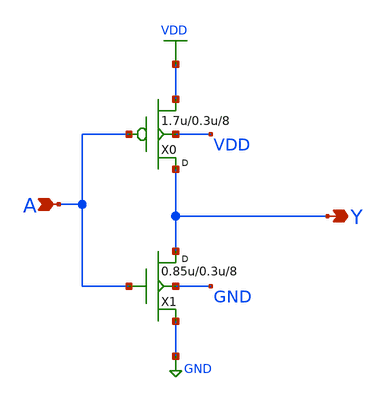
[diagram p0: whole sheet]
** sch_path: lib/12T/clkinv8/gf180mcu_osu_sc_clkinv_8.sch
**.subckt gf180mcu_osu_sc_clkinv_8 A Y
*.ipin A
*.opin Y
X0 Y A VDD VDD pmos_3p3 w=1.7u l=0.3u m=8
X1 Y A GND GND nmos_3p3 w=0.85u l=0.3u m=8
**.ends
.GLOBAL VDD
.GLOBAL GND
.end
